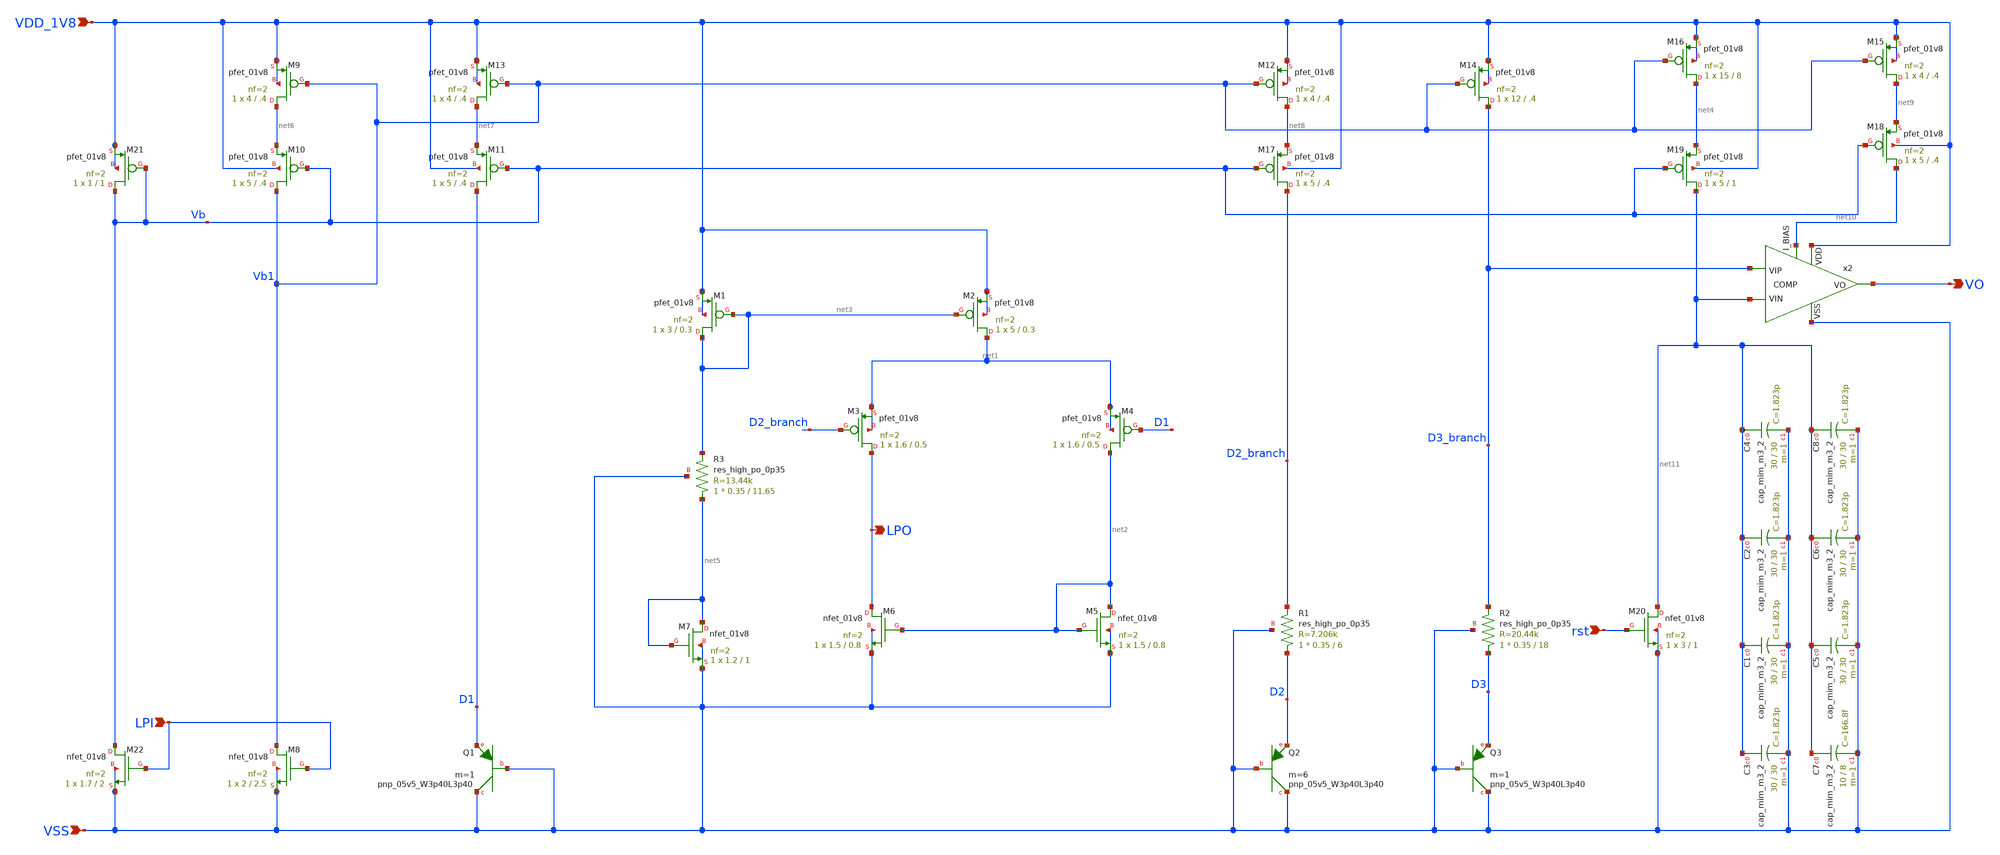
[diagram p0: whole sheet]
** sch_path: design/CNR_GR02_SKY130NM/CNR_GR02.sch
**.subckt CNR_GR02 VDD_1V8 VSS rst VO LPO LPI
*.ipin VDD_1V8
*.ipin VSS
*.ipin rst
*.opin VO
*.opin LPO
*.ipin LPI
x2 VDD_1V8 D3_branch net11 VO net10 VSS COMP
XQ2 VSS VSS D2 sky130_fd_pr__pnp_05v5_W3p40L3p40 m=6
XQ1 VSS VSS D1 sky130_fd_pr__pnp_05v5_W3p40L3p40 m=1
XM12 net8 Vb1 VDD_1V8 VDD_1V8 sky130_fd_pr__pfet_01v8 L=.4 W=4 nf=2 ad='int((nf+1)/2) * W/nf * 0.29'
+ as='int((nf+2)/2) * W/nf * 0.29' pd='2*int((nf+1)/2) * (W/nf + 0.29)' ps='2*int((nf+2)/2) * (W/nf + 0.29)'
+ nrd='0.29 / W' nrs='0.29 / W' sa=0 sb=0 sd=0 mult=1 m=1
XM13 net7 Vb1 VDD_1V8 VDD_1V8 sky130_fd_pr__pfet_01v8 L=.4 W=4 nf=2 ad='int((nf+1)/2) * W/nf * 0.29'
+ as='int((nf+2)/2) * W/nf * 0.29' pd='2*int((nf+1)/2) * (W/nf + 0.29)' ps='2*int((nf+2)/2) * (W/nf + 0.29)'
+ nrd='0.29 / W' nrs='0.29 / W' sa=0 sb=0 sd=0 mult=1 m=1
XM14 D3_branch Vb1 VDD_1V8 VDD_1V8 sky130_fd_pr__pfet_01v8 L=.4 W=12 nf=2 ad='int((nf+1)/2) * W/nf * 0.29'
+ as='int((nf+2)/2) * W/nf * 0.29' pd='2*int((nf+1)/2) * (W/nf + 0.29)' ps='2*int((nf+2)/2) * (W/nf + 0.29)'
+ nrd='0.29 / W' nrs='0.29 / W' sa=0 sb=0 sd=0 mult=1 m=1
XQ3 VSS VSS D3 sky130_fd_pr__pnp_05v5_W3p40L3p40 m=1
XM16 net4 Vb1 VDD_1V8 VDD_1V8 sky130_fd_pr__pfet_01v8 L=8 W=15 nf=2 ad='int((nf+1)/2) * W/nf * 0.29'
+ as='int((nf+2)/2) * W/nf * 0.29' pd='2*int((nf+1)/2) * (W/nf + 0.29)' ps='2*int((nf+2)/2) * (W/nf + 0.29)'
+ nrd='0.29 / W' nrs='0.29 / W' sa=0 sb=0 sd=0 mult=1 m=1
XM1 net3 net3 VDD_1V8 VDD_1V8 sky130_fd_pr__pfet_01v8 L=0.3 W=3 nf=2 ad='int((nf+1)/2) * W/nf * 0.29'
+ as='int((nf+2)/2) * W/nf * 0.29' pd='2*int((nf+1)/2) * (W/nf + 0.29)' ps='2*int((nf+2)/2) * (W/nf + 0.29)'
+ nrd='0.29 / W' nrs='0.29 / W' sa=0 sb=0 sd=0 mult=1 m=1
XM2 net1 net3 VDD_1V8 VDD_1V8 sky130_fd_pr__pfet_01v8 L=0.3 W=5 nf=2 ad='int((nf+1)/2) * W/nf * 0.29'
+ as='int((nf+2)/2) * W/nf * 0.29' pd='2*int((nf+1)/2) * (W/nf + 0.29)' ps='2*int((nf+2)/2) * (W/nf + 0.29)'
+ nrd='0.29 / W' nrs='0.29 / W' sa=0 sb=0 sd=0 mult=1 m=1
XM3 LPO D2_branch net1 net1 sky130_fd_pr__pfet_01v8 L=0.5 W=1.6 nf=2 ad='int((nf+1)/2) * W/nf * 0.29'
+ as='int((nf+2)/2) * W/nf * 0.29' pd='2*int((nf+1)/2) * (W/nf + 0.29)' ps='2*int((nf+2)/2) * (W/nf + 0.29)'
+ nrd='0.29 / W' nrs='0.29 / W' sa=0 sb=0 sd=0 mult=1 m=1
XM4 net2 D1 net1 net1 sky130_fd_pr__pfet_01v8 L=0.5 W=1.6 nf=2 ad='int((nf+1)/2) * W/nf * 0.29' as='int((nf+2)/2) * W/nf * 0.29'
+ pd='2*int((nf+1)/2) * (W/nf + 0.29)' ps='2*int((nf+2)/2) * (W/nf + 0.29)' nrd='0.29 / W' nrs='0.29 / W'
+ sa=0 sb=0 sd=0 mult=1 m=1
XM5 net2 net2 VSS VSS sky130_fd_pr__nfet_01v8 L=0.8 W=1.5 nf=2 ad='int((nf+1)/2) * W/nf * 0.29' as='int((nf+2)/2) * W/nf * 0.29'
+ pd='2*int((nf+1)/2) * (W/nf + 0.29)' ps='2*int((nf+2)/2) * (W/nf + 0.29)' nrd='0.29 / W' nrs='0.29 / W'
+ sa=0 sb=0 sd=0 mult=1 m=1
XM6 LPO net2 VSS VSS sky130_fd_pr__nfet_01v8 L=0.8 W=1.5 nf=2 ad='int((nf+1)/2) * W/nf * 0.29' as='int((nf+2)/2) * W/nf * 0.29'
+ pd='2*int((nf+1)/2) * (W/nf + 0.29)' ps='2*int((nf+2)/2) * (W/nf + 0.29)' nrd='0.29 / W' nrs='0.29 / W'
+ sa=0 sb=0 sd=0 mult=1 m=1
XR2 D3 D3_branch VSS sky130_fd_pr__res_high_po_0p35 L=18 mult=1 m=1
XR1 D2 D2_branch VSS sky130_fd_pr__res_high_po_0p35 L=6 mult=1 m=1
XM7 net5 net5 VSS VSS sky130_fd_pr__nfet_01v8 L=1 W=1.2 nf=2 ad='int((nf+1)/2) * W/nf * 0.29' as='int((nf+2)/2) * W/nf * 0.29'
+ pd='2*int((nf+1)/2) * (W/nf + 0.29)' ps='2*int((nf+2)/2) * (W/nf + 0.29)' nrd='0.29 / W' nrs='0.29 / W'
+ sa=0 sb=0 sd=0 mult=1 m=1
XR3 net5 net3 VSS sky130_fd_pr__res_high_po_0p35 L=11.65 mult=1 m=1
XM8 Vb1 LPI VSS VSS sky130_fd_pr__nfet_01v8 L=2.5 W=2 nf=2 ad='int((nf+1)/2) * W/nf * 0.29' as='int((nf+2)/2) * W/nf * 0.29'
+ pd='2*int((nf+1)/2) * (W/nf + 0.29)' ps='2*int((nf+2)/2) * (W/nf + 0.29)' nrd='0.29 / W' nrs='0.29 / W'
+ sa=0 sb=0 sd=0 mult=1 m=1
XM9 net6 Vb1 VDD_1V8 VDD_1V8 sky130_fd_pr__pfet_01v8 L=.4 W=4 nf=2 ad='int((nf+1)/2) * W/nf * 0.29' as='int((nf+2)/2) * W/nf * 0.29'
+ pd='2*int((nf+1)/2) * (W/nf + 0.29)' ps='2*int((nf+2)/2) * (W/nf + 0.29)' nrd='0.29 / W' nrs='0.29 / W'
+ sa=0 sb=0 sd=0 mult=1 m=1
XM10 Vb1 Vb net6 VDD_1V8 sky130_fd_pr__pfet_01v8 L=.4 W=5 nf=2 ad='int((nf+1)/2) * W/nf * 0.29' as='int((nf+2)/2) * W/nf * 0.29'
+ pd='2*int((nf+1)/2) * (W/nf + 0.29)' ps='2*int((nf+2)/2) * (W/nf + 0.29)' nrd='0.29 / W' nrs='0.29 / W'
+ sa=0 sb=0 sd=0 mult=1 m=1
XM11 D1 Vb net7 VDD_1V8 sky130_fd_pr__pfet_01v8 L=.4 W=5 nf=2 ad='int((nf+1)/2) * W/nf * 0.29' as='int((nf+2)/2) * W/nf * 0.29'
+ pd='2*int((nf+1)/2) * (W/nf + 0.29)' ps='2*int((nf+2)/2) * (W/nf + 0.29)' nrd='0.29 / W' nrs='0.29 / W'
+ sa=0 sb=0 sd=0 mult=1 m=1
XM17 D2_branch Vb net8 VDD_1V8 sky130_fd_pr__pfet_01v8 L=.4 W=5 nf=2 ad='int((nf+1)/2) * W/nf * 0.29'
+ as='int((nf+2)/2) * W/nf * 0.29' pd='2*int((nf+1)/2) * (W/nf + 0.29)' ps='2*int((nf+2)/2) * (W/nf + 0.29)'
+ nrd='0.29 / W' nrs='0.29 / W' sa=0 sb=0 sd=0 mult=1 m=1
XM21 Vb Vb VDD_1V8 VDD_1V8 sky130_fd_pr__pfet_01v8 L=1 W=1 nf=2 ad='int((nf+1)/2) * W/nf * 0.29' as='int((nf+2)/2) * W/nf * 0.29'
+ pd='2*int((nf+1)/2) * (W/nf + 0.29)' ps='2*int((nf+2)/2) * (W/nf + 0.29)' nrd='0.29 / W' nrs='0.29 / W'
+ sa=0 sb=0 sd=0 mult=1 m=1
XM22 Vb LPI VSS VSS sky130_fd_pr__nfet_01v8 L=2 W=1.7 nf=2 ad='int((nf+1)/2) * W/nf * 0.29' as='int((nf+2)/2) * W/nf * 0.29'
+ pd='2*int((nf+1)/2) * (W/nf + 0.29)' ps='2*int((nf+2)/2) * (W/nf + 0.29)' nrd='0.29 / W' nrs='0.29 / W'
+ sa=0 sb=0 sd=0 mult=1 m=1
XM20 net11 rst VSS VSS sky130_fd_pr__nfet_01v8 L=1 W=3 nf=2 ad='int((nf+1)/2) * W/nf * 0.29' as='int((nf+2)/2) * W/nf * 0.29'
+ pd='2*int((nf+1)/2) * (W/nf + 0.29)' ps='2*int((nf+2)/2) * (W/nf + 0.29)' nrd='0.29 / W' nrs='0.29 / W'
+ sa=0 sb=0 sd=0 mult=1 m=1
XM15 net9 Vb1 VDD_1V8 VDD_1V8 sky130_fd_pr__pfet_01v8 L=.4 W=4 nf=2 ad='int((nf+1)/2) * W/nf * 0.29'
+ as='int((nf+2)/2) * W/nf * 0.29' pd='2*int((nf+1)/2) * (W/nf + 0.29)' ps='2*int((nf+2)/2) * (W/nf + 0.29)'
+ nrd='0.29 / W' nrs='0.29 / W' sa=0 sb=0 sd=0 mult=1 m=1
XM18 net10 Vb net9 VDD_1V8 sky130_fd_pr__pfet_01v8 L=.4 W=5 nf=2 ad='int((nf+1)/2) * W/nf * 0.29' as='int((nf+2)/2) * W/nf * 0.29'
+ pd='2*int((nf+1)/2) * (W/nf + 0.29)' ps='2*int((nf+2)/2) * (W/nf + 0.29)' nrd='0.29 / W' nrs='0.29 / W'
+ sa=0 sb=0 sd=0 mult=1 m=1
XM19 net11 Vb net4 VDD_1V8 sky130_fd_pr__pfet_01v8 L=1 W=5 nf=2 ad='int((nf+1)/2) * W/nf * 0.29' as='int((nf+2)/2) * W/nf * 0.29'
+ pd='2*int((nf+1)/2) * (W/nf + 0.29)' ps='2*int((nf+2)/2) * (W/nf + 0.29)' nrd='0.29 / W' nrs='0.29 / W'
+ sa=0 sb=0 sd=0 mult=1 m=1
XC1 net11 VSS sky130_fd_pr__cap_mim_m3_2 W=30 L=30 MF=1 m=1
XC2 net11 VSS sky130_fd_pr__cap_mim_m3_2 W=30 L=30 MF=1 m=1
XC3 net11 VSS sky130_fd_pr__cap_mim_m3_2 W=30 L=30 MF=1 m=1
XC4 net11 VSS sky130_fd_pr__cap_mim_m3_2 W=30 L=30 MF=1 m=1
XC5 net11 VSS sky130_fd_pr__cap_mim_m3_2 W=30 L=30 MF=1 m=1
XC6 net11 VSS sky130_fd_pr__cap_mim_m3_2 W=30 L=30 MF=1 m=1
XC7 net11 VSS sky130_fd_pr__cap_mim_m3_2 W=10 L=8 MF=1 m=1
XC8 net11 VSS sky130_fd_pr__cap_mim_m3_2 W=30 L=30 MF=1 m=1
**.ends
.end
